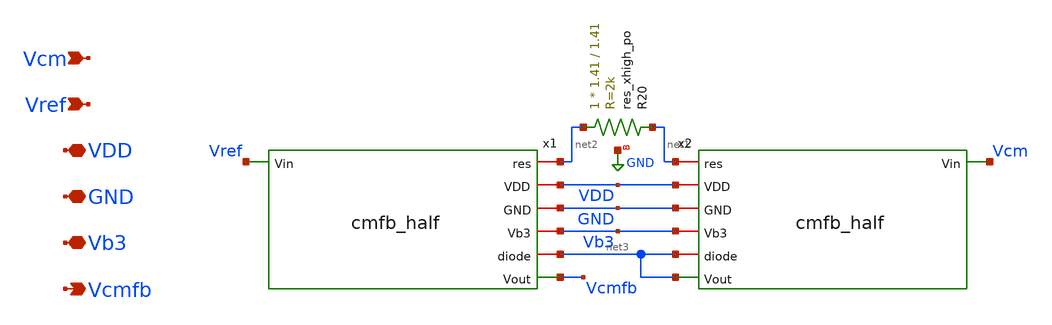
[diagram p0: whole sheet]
** sch_path: xschem/cmfb.sch
**.subckt cmfb VDD GND Vcmfb Vref Vb3 Vcm
*.iopin VDD
*.iopin GND
*.opin Vcmfb
*.ipin Vref
*.iopin Vb3
*.ipin Vcm
x1 Vref net2 VDD GND Vb3 net3 Vcmfb cmfb_half
x2 Vcm net1 VDD GND Vb3 net3 net3 cmfb_half
XR20 net2 net1 GND sky130_fd_pr__res_xhigh_po W=1.41 L=1.41 mult=1 m=1
**.ends

* expanding   symbol:  tia_post_approval/schem/cmfb_half.sym # of pins=7
** sym_path: tia_post_approval/schem/cmfb_half.sym
** sch_path: tia_post_approval/schem/cmfb_half.sch
.subckt cmfb_half Vin res VDD GND Vb3 diode Vout
*.iopin VDD
*.iopin GND
*.opin Vout
*.ipin Vin
*.iopin diode
*.iopin Vb3
*.iopin res
XM11 Vout Vin res GND sky130_fd_pr__nfet_01v8 L=0.20 W=150 nf=2 ad='int((nf+1)/2) * W/nf * 0.29' as='int((nf+2)/2) * W/nf * 0.29'
+ pd='2*int((nf+1)/2) * (W/nf + 0.29)' ps='2*int((nf+2)/2) * (W/nf + 0.29)' nrd='0.29 / W' nrs='0.29 / W'
+ sa=0 sb=0 sd=0 mult=1 m=1
XM14 Vout diode VDD VDD sky130_fd_pr__pfet_01v8 L=0.2 W=42 nf=1 ad='int((nf+1)/2) * W/nf * 0.29' as='int((nf+2)/2) * W/nf * 0.29'
+ pd='2*int((nf+1)/2) * (W/nf + 0.29)' ps='2*int((nf+2)/2) * (W/nf + 0.29)' nrd='0.29 / W' nrs='0.29 / W'
+ sa=0 sb=0 sd=0 mult=1 m=1
XM15 res Vb3 GND GND sky130_fd_pr__nfet_01v8 L=.5 W=65 nf=1 ad='int((nf+1)/2) * W/nf * 0.29' as='int((nf+2)/2) * W/nf * 0.29'
+ pd='2*int((nf+1)/2) * (W/nf + 0.29)' ps='2*int((nf+2)/2) * (W/nf + 0.29)' nrd='0.29 / W' nrs='0.29 / W'
+ sa=0 sb=0 sd=0 mult=1 m=1
.ends

.GLOBAL GND
.end
